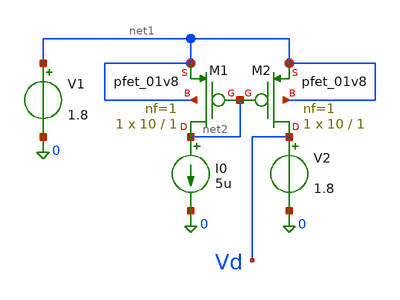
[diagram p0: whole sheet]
** sch_path: stage1/schematics/current_mirror.sch
**.subckt current_mirror
I0 net2 0 5u
XM1 net2 net2 net1 net1 sky130_fd_pr__pfet_01v8 L=1 W=10 nf=1 ad='int((1 + 1)/2) * 10 / 1 * 0.29' as='int((1 + 2)/2) * 10 / 1 * 0.29'
+ pd='2*int((1 + 1)/2) * (10 / 1 + 0.29)' ps='2*int((1 + 2)/2) * (10 / 1 + 0.29)' nrd='0.29 / 10 ' nrs='0.29 / 10 '
+ sa=0 sb=0 sd=0 mult=1 m=1
XM2 Vd net2 net1 net1 sky130_fd_pr__pfet_01v8 L=1 W=10 nf=1 ad='int((1 + 1)/2) * 10 / 1 * 0.29' as='int((1 + 2)/2) * 10 / 1 * 0.29'
+ pd='2*int((1 + 1)/2) * (10 / 1 + 0.29)' ps='2*int((1 + 2)/2) * (10 / 1 + 0.29)' nrd='0.29 / 10 ' nrs='0.29 / 10 '
+ sa=0 sb=0 sd=0 mult=1 m=1
V1 net1 0 1.8
V2 Vd 0 1.8
**** begin user architecture code

.options savecurrents

.control
	save all
	dc V2 1.8 0 -0.01
	let vsd = 1.8 - v(Vd)
	let id = V2#branch
	plot id vs vsd
.endc


** opencircuitdesign pdks install
.lib $::SKYWATER_MODELS/sky130.lib.spice tt

**** end user architecture code
**.ends
.end
